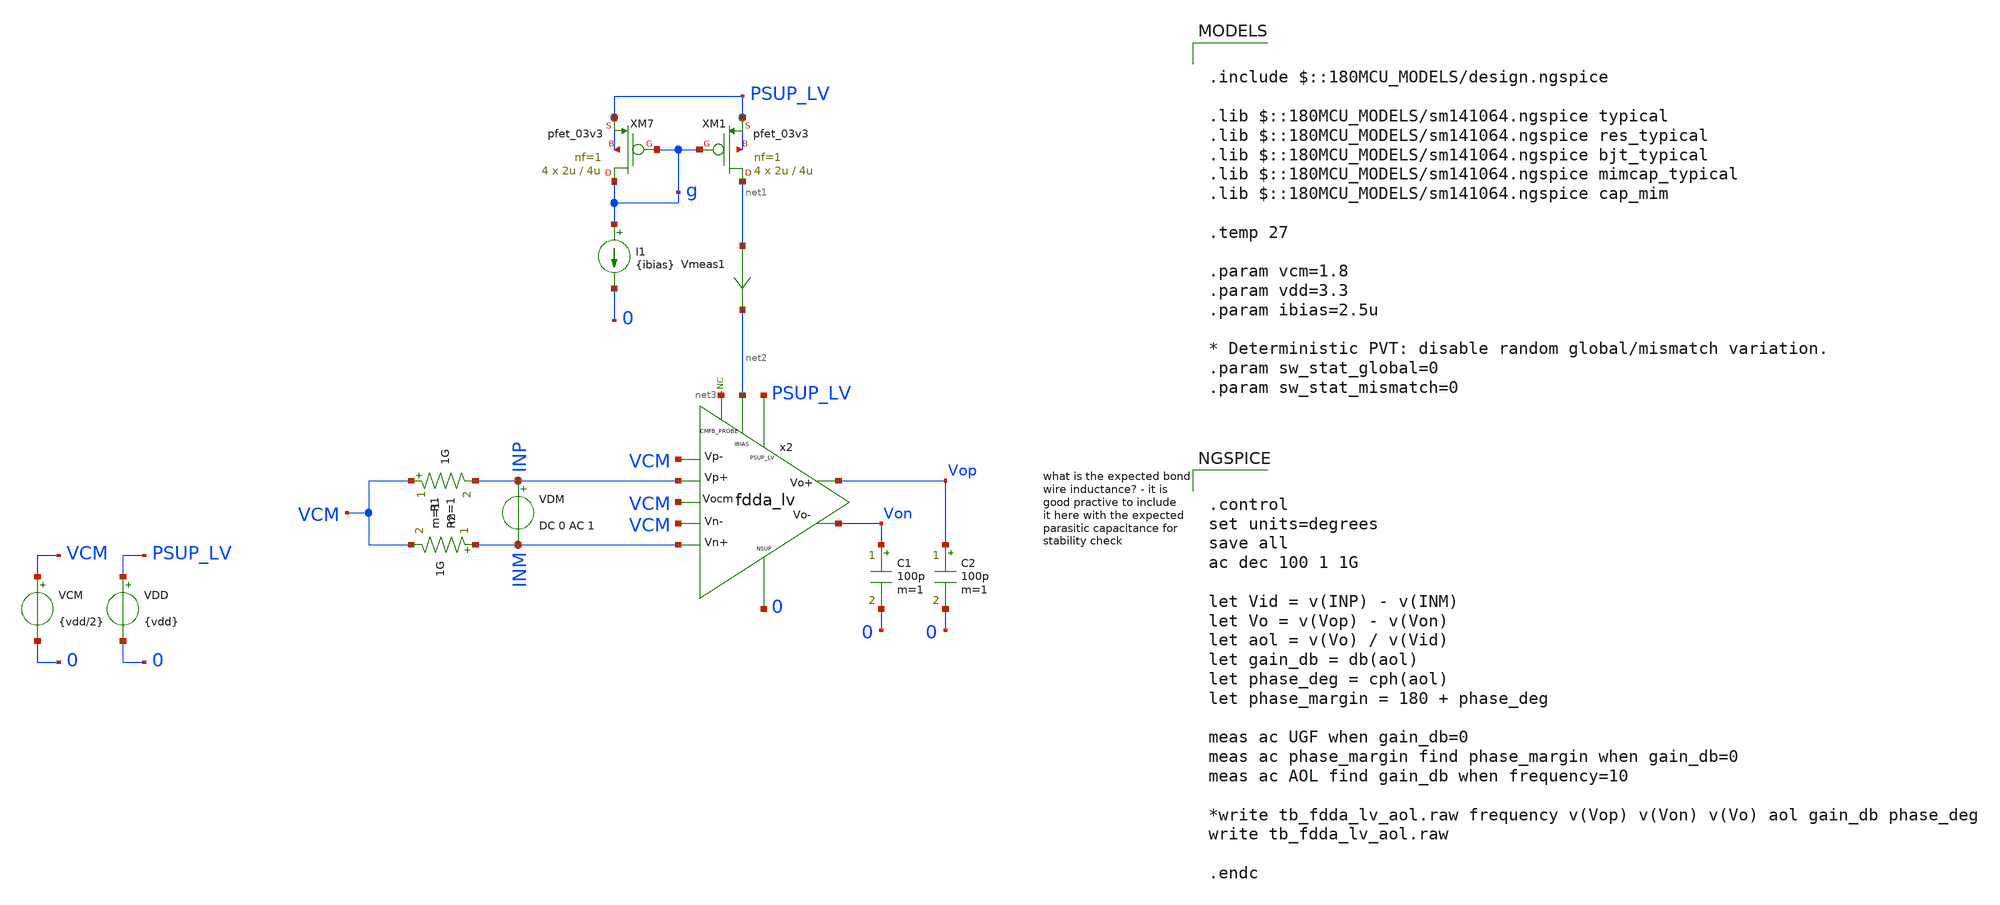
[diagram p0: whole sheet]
** sch_path: xschem/blocks/fdda_lv/tb_fdda_lv_aol.sch
**.subckt tb_fdda_lv_aol
C1 Von 0 100p m=1
x2 PSUP_LV VCM VCM INM INP Vop Von net2 0 net3 VCM fdda_lv
VDD PSUP_LV 0 {vdd}
C2 Vop 0 100p m=1
VCM VCM 0 {vdd/2}
* noconn #net3
VDM INP INM DC 0 AC 1
R1 VCM INP 1G m=1
R2 INM VCM 1G m=1
XM7 g g PSUP_LV PSUP_LV pfet_03v3 L=4u W=2u nf=1 ad='int((nf+1)/2) * W/nf * 0.18u' as='int((nf+2)/2) * W/nf * 0.18u'
+ pd='2*int((nf+1)/2) * (W/nf + 0.18u)' ps='2*int((nf+2)/2) * (W/nf + 0.18u)' nrd='0.18u / W' nrs='0.18u / W'
+ sa=0 sb=0 sd=0 m=4
XM1 net1 g PSUP_LV PSUP_LV pfet_03v3 L=4u W=2u nf=1 ad='int((nf+1)/2) * W/nf * 0.18u' as='int((nf+2)/2) * W/nf * 0.18u'
+ pd='2*int((nf+1)/2) * (W/nf + 0.18u)' ps='2*int((nf+2)/2) * (W/nf + 0.18u)' nrd='0.18u / W' nrs='0.18u / W'
+ sa=0 sb=0 sd=0 m=4
I1 g 0 {ibias}
Vmeas1 net1 net2 0
.save i(vmeas1)
**** begin user architecture code

.include $::180MCU_MODELS/design.ngspice

.lib $::180MCU_MODELS/sm141064.ngspice typical
.lib $::180MCU_MODELS/sm141064.ngspice res_typical
.lib $::180MCU_MODELS/sm141064.ngspice bjt_typical
.lib $::180MCU_MODELS/sm141064.ngspice mimcap_typical
.lib $::180MCU_MODELS/sm141064.ngspice cap_mim

.temp 27

.param vcm=1.8
.param vdd=3.3
.param ibias=2.5u

* Deterministic PVT: disable random global/mismatch variation.
.param sw_stat_global=0
.param sw_stat_mismatch=0



.control
set units=degrees
save all
ac dec 100 1 1G

let Vid = v(INP) - v(INM)
let Vo = v(Vop) - v(Von)
let aol = v(Vo) / v(Vid)
let gain_db = db(aol)
let phase_deg = cph(aol)
let phase_margin = 180 + phase_deg

meas ac UGF when gain_db=0
meas ac phase_margin find phase_margin when gain_db=0
meas ac AOL find gain_db when frequency=10

*write tb_fdda_lv_aol.raw frequency v(Vop) v(Von) v(Vo) aol gain_db phase_deg
write tb_fdda_lv_aol.raw

.endc


**** end user architecture code
**.ends
.end
